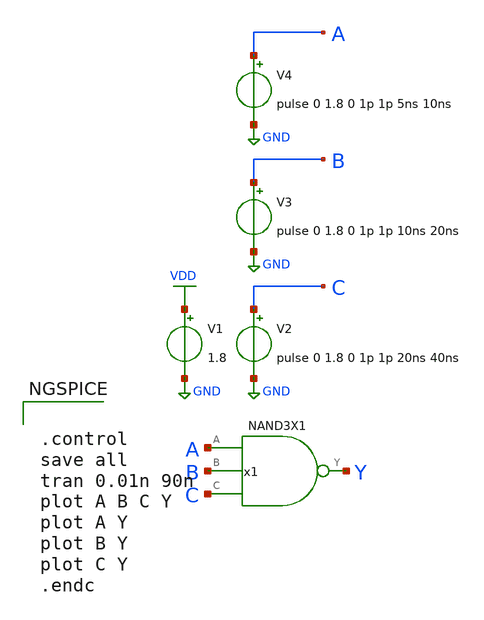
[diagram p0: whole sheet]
** sch_path: lib/xschem/test_NAND3X1.sch
**.subckt test_NAND3X1
V2 C GND pulse 0 1.8 0 1p 1p 20ns 40ns
V1 VDD GND 1.8
V3 B GND pulse 0 1.8 0 1p 1p 10ns 20ns
V4 A GND pulse 0 1.8 0 1p 1p 5ns 10ns
x1 Y A B C VDD GND NAND3X1
**** begin user architecture code

.lib $::SKYWATER_MODELS/sky130.lib.spice tt


**** end user architecture code
**.ends
.GLOBAL VDD
.GLOBAL GND
**** begin user architecture code


.control
save all
tran 0.01n 90n
plot A B C Y
plot A Y
plot B Y
plot C Y
.endc


**** end user architecture code
.end
